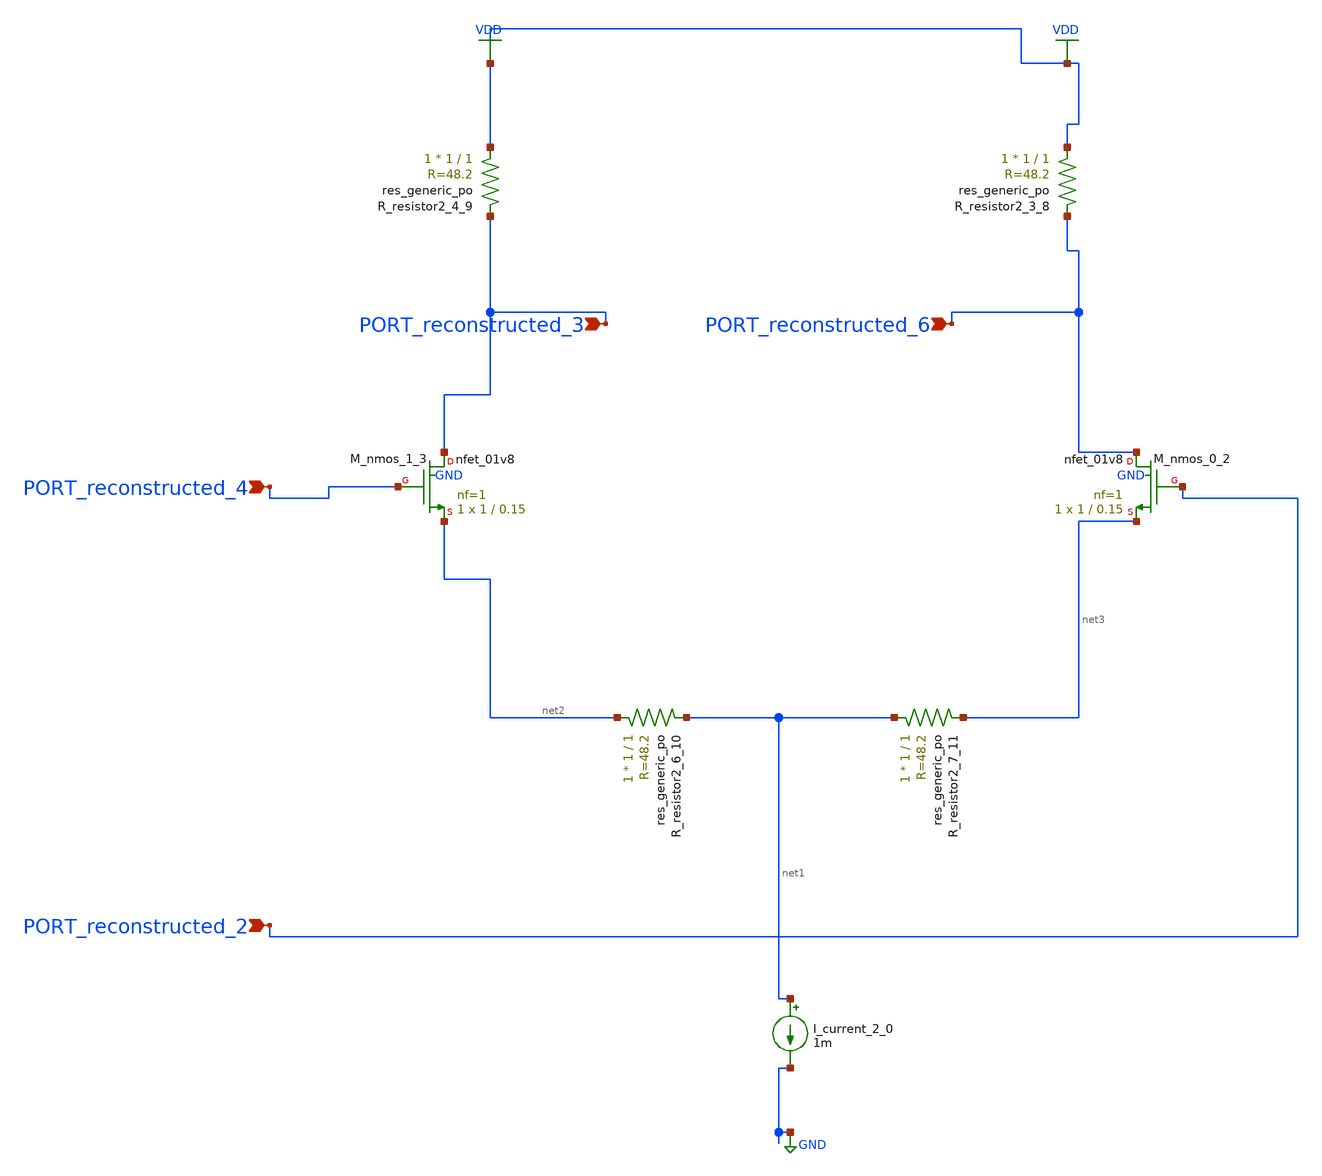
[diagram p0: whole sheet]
** sch_path: schematics/AMSNet/805.sch
**.subckt 805 PORT_reconstructed_6 PORT_reconstructed_2 PORT_reconstructed_3 PORT_reconstructed_4
*.ipin PORT_reconstructed_6
*.ipin PORT_reconstructed_2
*.ipin PORT_reconstructed_3
*.ipin PORT_reconstructed_4
I_current_2_0 net1 GND 1m
XM_nmos_0_2 PORT_reconstructed_6 PORT_reconstructed_2 net3 GND sky130_fd_pr__nfet_01v8 L=0.15 W=1 nf=1
+ ad='int((1 + 1)/2) * 1 / 1 * 0.29' as='int((1 + 2)/2) * 1 / 1 * 0.29' pd='2*int((1 + 1)/2) * (1 / 1 + 0.29)'
+ ps='2*int((1 + 2)/2) * (1 / 1 + 0.29)' nrd='0.29 / 1 ' nrs='0.29 / 1 ' sa=0 sb=0 sd=0 mult=1 m=1
XM_nmos_1_3 PORT_reconstructed_3 PORT_reconstructed_4 net2 GND sky130_fd_pr__nfet_01v8 L=0.15 W=1 nf=1
+ ad='int((1 + 1)/2) * 1 / 1 * 0.29' as='int((1 + 2)/2) * 1 / 1 * 0.29' pd='2*int((1 + 1)/2) * (1 / 1 + 0.29)'
+ ps='2*int((1 + 2)/2) * (1 / 1 + 0.29)' nrd='0.29 / 1 ' nrs='0.29 / 1 ' sa=0 sb=0 sd=0 mult=1 m=1
XR_resistor2_3_8 VDD PORT_reconstructed_6 sky130_fd_pr__res_generic_po W=1 L=1 m=1
XR_resistor2_4_9 VDD PORT_reconstructed_3 sky130_fd_pr__res_generic_po W=1 L=1 m=1
XR_resistor2_6_10 net2 net1 sky130_fd_pr__res_generic_po W=1 L=1 m=1
XR_resistor2_7_11 net1 net3 sky130_fd_pr__res_generic_po W=1 L=1 m=1
**.ends
.GLOBAL GND
.GLOBAL VDD
.end
